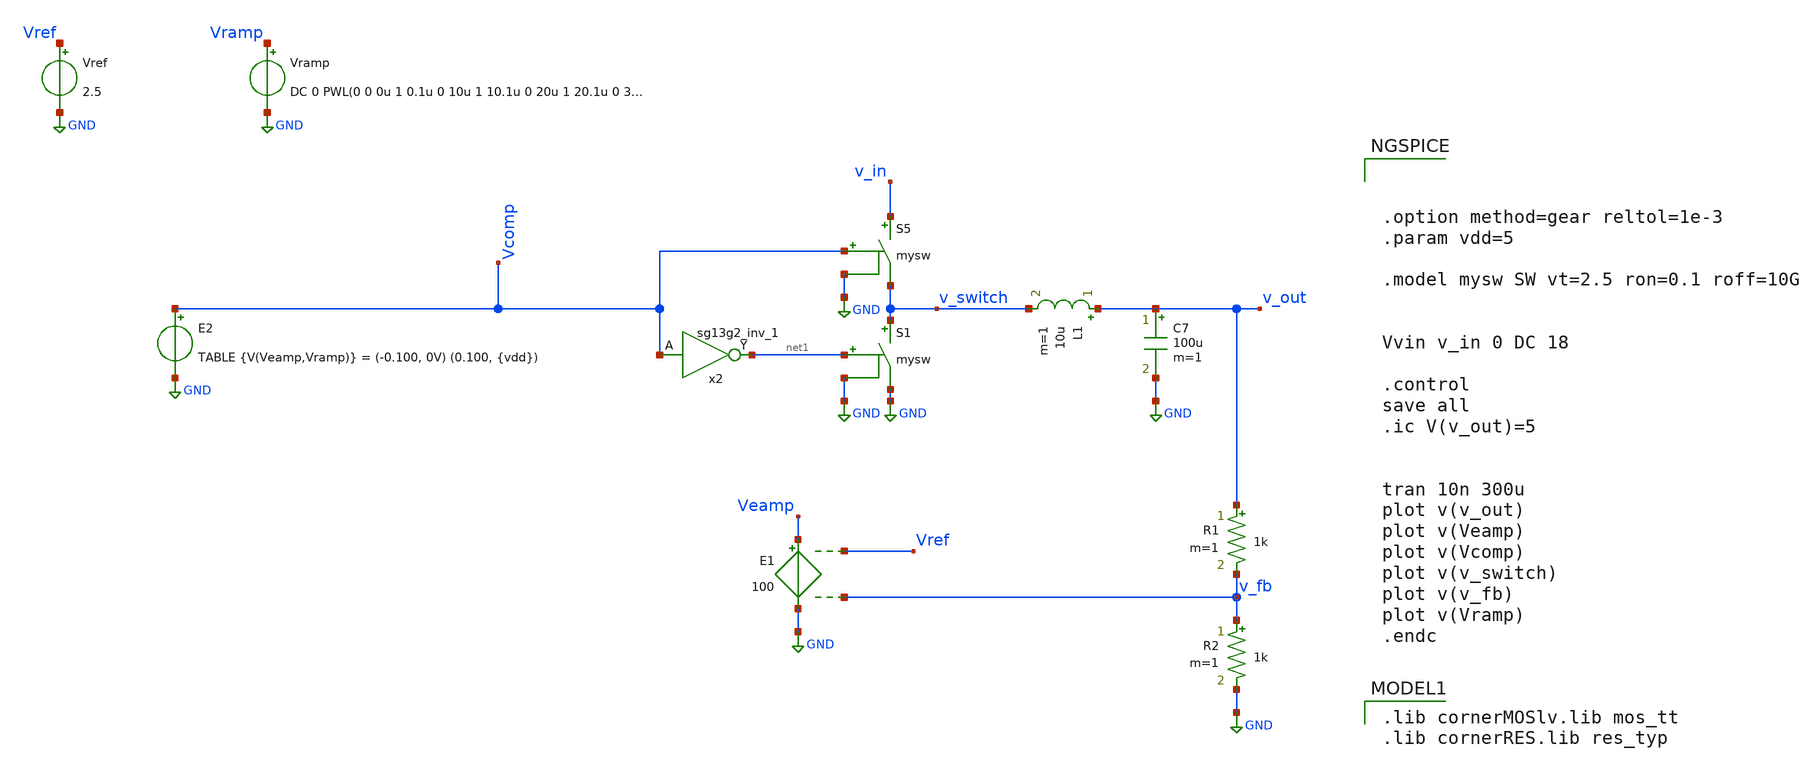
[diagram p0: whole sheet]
** sch_path: Designs/ideal_circuits/ideal_dcdc.sch
* (c) 2025 Thesis_HP, Apache-2.0 license
**.subckt ideal_dcdc
Vramp Vramp GND DC 0 PWL(0 0 0u 1 0.1u 0 10u 1 10.1u 0 20u 1 20.1u 0 30u 1 30.1u 0 40u 1 40.1u 0 50u
+ 1 50.1u 0 60u 1 60.1u 0 70u 1 70.1u 0 80u 1 80.1u 0 90u 1 90.1u 0 100u 1 100.1u 0 110u 1 110.1u 0
+ 120u 1 120.1u 0 130u 1 130.1u 0 140u 1 140.1u 0 150u 1 150.1u 0 160u 1 160.1u 0 170u 1 170.1u 0 180u 1
+ 180.1u 0 190u 1 190.1u 0 200u 1 200.1u 0 210u 1 210.1u 0 220u 1 220.1u 0 230u 1 230.1u 0 240u 1 240.1u 0
+ 250u 1 250.1u 0 260u 1 260.1u 0 270u 1 270.1u 0 280u 1 280.1u 0 290u 1 290.1u 0 300u 1)
S5 v_in v_switch Vcomp GND mysw
S1 v_switch GND net1 GND mysw
L1 v_out v_switch 10u m=1
C7 v_out GND 100u m=1
R1 v_out v_fb 1k m=1
R2 v_fb GND 1k m=1
Vref Vref GND 2.5
x2 net1 Vcomp 1.5 0 sg13g2_inv_1
E1 Veamp GND Vref v_fb 100
E2 Vcomp GND TABLE {V(Veamp,Vramp)} = (-0.100, 0V) (0.100, {vdd})
**** begin user architecture code



.option method=gear reltol=1e-3
.param vdd=5

.model mysw SW vt=2.5 ron=0.1 roff=10G


Vvin v_in 0 DC 18

.control
save all
.ic V(v_out)=5


tran 10n 300u
plot v(v_out)
plot v(Veamp)
plot v(Vcomp)
plot v(v_switch)
plot v(v_fb)
plot v(Vramp)
.endc


 .lib cornerMOSlv.lib mos_tt
.lib cornerRES.lib res_typ


.lib $::SG13G2_MODELS/cornerMOSlv.lib mos_tt
.lib $::SG13G2_MODELS/cornerRES.lib res_typ
.inc /foss/pdks/ihp-sg13g2/libs.ref/sg13g2_stdcell/spice/sg13g2_stdcell.spice

**** end user architecture code
**.ends

* expanding   symbol:  sg13g2_stdcells/sg13g2_inv_1.sym # of pins=2
** sym_path: sg13g2_stdcells/sg13g2_inv_1.sym
** sch_path: sg13g2_stdcells/sg13g2_inv_1.sch
.subckt sg13g2_inv_1 Y A VDD VSS
*.opin Y
*.ipin A
*.iopin VDD
*.iopin VSS
XM1 Y A VSS VSS sg13_lv_nmos w=740.00n l=130.00n ng=1 m=1 mm_ok=1
XM2 Y A VDD VDD sg13_lv_pmos w=1.12u l=130.00n ng=1 m=1 mm_ok=1
.ends

.GLOBAL GND
.end
